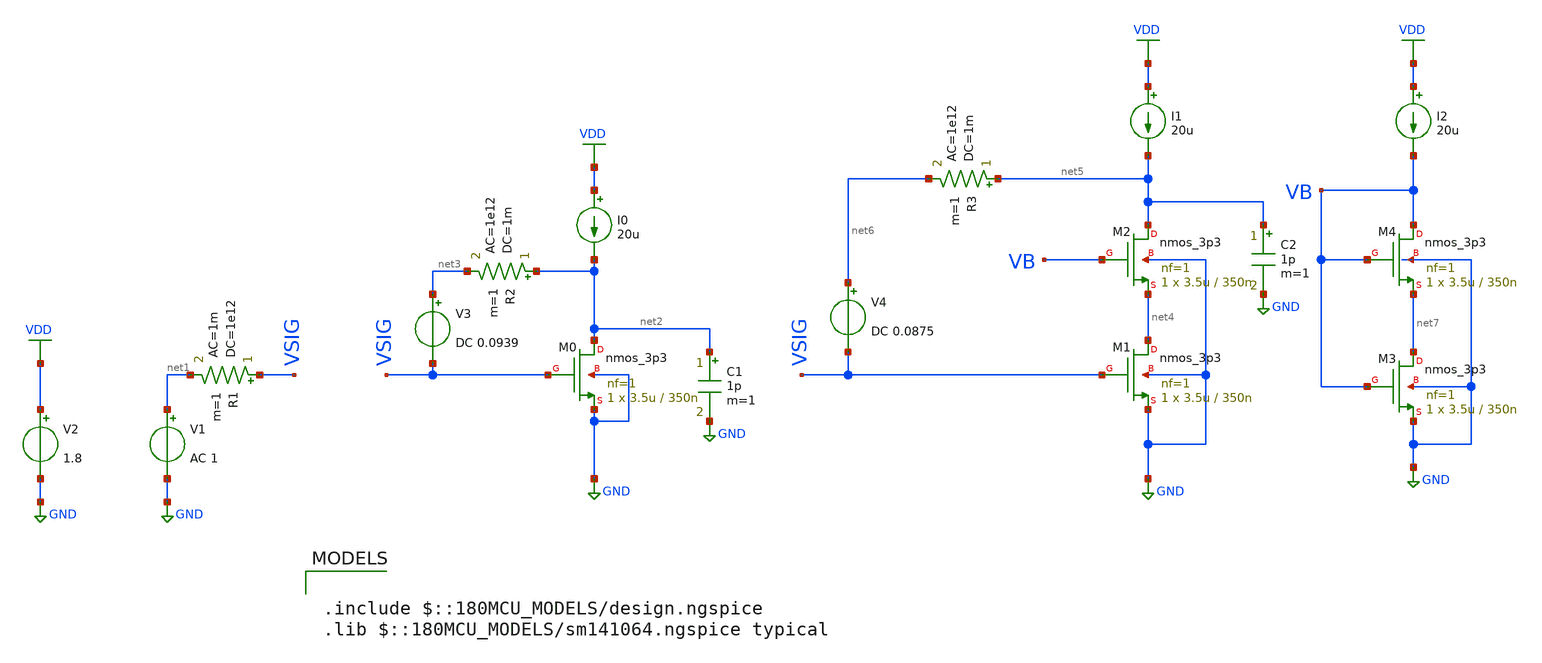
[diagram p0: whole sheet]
** sch_path: ITI_Labs/Lab3/Design/Lab03.sch
**.subckt Lab03
V1 net1 GND AC 1
R1 VSIG net1 1e12 ac=1m m=1
XM0 net2 VSIG GND GND nmos_3p3 L=350n W=3.5u nf=1 ad='int((nf+1)/2) * W/nf * 0.18u' as='int((nf+2)/2) * W/nf * 0.18u'
+ pd='2*int((nf+1)/2) * (W/nf + 0.18u)' ps='2*int((nf+2)/2) * (W/nf + 0.18u)' nrd='0.18u / W' nrs='0.18u / W'
+ sa=0 sb=0 sd=0 m=1
I0 VDD net2 20u
C1 net2 GND 1p m=1
V2 VDD GND 1.8
V3 net3 VSIG DC 0.0939
R2 net2 net3 1m ac=1e12 m=1
XM1 net4 VSIG GND GND nmos_3p3 L=350n W=3.5u nf=1 ad='int((nf+1)/2) * W/nf * 0.18u' as='int((nf+2)/2) * W/nf * 0.18u'
+ pd='2*int((nf+1)/2) * (W/nf + 0.18u)' ps='2*int((nf+2)/2) * (W/nf + 0.18u)' nrd='0.18u / W' nrs='0.18u / W'
+ sa=0 sb=0 sd=0 m=1
XM2 net5 VB net4 GND nmos_3p3 L=350n W=3.5u nf=1 ad='int((nf+1)/2) * W/nf * 0.18u' as='int((nf+2)/2) * W/nf * 0.18u'
+ pd='2*int((nf+1)/2) * (W/nf + 0.18u)' ps='2*int((nf+2)/2) * (W/nf + 0.18u)' nrd='0.18u / W' nrs='0.18u / W'
+ sa=0 sb=0 sd=0 m=1
V4 net6 VSIG DC 0.0875
I1 VDD net5 20u
R3 net5 net6 1m ac=1e12 m=1
C2 net5 GND 1p m=1
XM4 VB VB net7 GND nmos_3p3 L=350n W=3.5u nf=1 ad='int((nf+1)/2) * W/nf * 0.18u' as='int((nf+2)/2) * W/nf * 0.18u'
+ pd='2*int((nf+1)/2) * (W/nf + 0.18u)' ps='2*int((nf+2)/2) * (W/nf + 0.18u)' nrd='0.18u / W' nrs='0.18u / W'
+ sa=0 sb=0 sd=0 m=1
I2 VDD VB 20u
XM3 net7 VB GND GND nmos_3p3 L=350n W=3.5u nf=1 ad='int((nf+1)/2) * W/nf * 0.18u' as='int((nf+2)/2) * W/nf * 0.18u'
+ pd='2*int((nf+1)/2) * (W/nf + 0.18u)' ps='2*int((nf+2)/2) * (W/nf + 0.18u)' nrd='0.18u / W' nrs='0.18u / W'
+ sa=0 sb=0 sd=0 m=1
**** begin user architecture code

.include $::180MCU_MODELS/design.ngspice
.lib $::180MCU_MODELS/sm141064.ngspice typical



.control
save all  @m.xm0.m0[id]  @m.xm0.m0[vgs]  @m.xm0.m0[vds]  @m.xm0.m0[vth]  @m.xm0.m0[vdssat]
+  @m.xm0.m0[gm]  @m.xm0.m0[gds]  @m.xm0.m0[gmbs]  @m.xm0.m0[cdb]  @m.xm0.m0[cgd]  @m.xm0.m0[cgs]  @m.xm0.m0[csb]
  @m.xm1.m0[id]  @m.xm1.m0[vgs]  @m.xm1.m0[vds]  @m.xm1.m0[vth]  @m.xm1.m0[vdssat]  @m.xm1.m0[gm]
+  @m.xm1.m0[gds]  @m.xm1.m0[gmbs]  @m.xm1.m0[cdb]  @m.xm1.m0[cgd]  @m.xm1.m0[cgs]  @m.xm1.m0[csb]

  @m.xm2.m0[id]  @m.xm2.m0[vgs]  @m.xm2.m0[vds]  @m.xm2.m0[vth]  @m.xm2.m0[vdssat]  @m.xm2.m0[gm]
+  @m.xm2.m0[gds]  @m.xm2.m0[gmbs]  @m.xm2.m0[cdb]  @m.xm2.m0[cgd]  @m.xm2.m0[cgs]  @m.xm2.m0[csb]

  @m.xm3.m0[id]  @m.xm3.m0[vgs]  @m.xm3.m0[vds]  @m.xm3.m0[vth]  @m.xm3.m0[vdssat]  @m.xm3.m0[gm]
+  @m.xm3.m0[gds]  @m.xm3.m0[gmbs]  @m.xm3.m0[cdb]  @m.xm3.m0[cgd]  @m.xm3.m0[cgs]  @m.xm3.m0[csb]
  @m.xm4.m0[id]  @m.xm4.m0[vgs]  @m.xm4.m0[vds]  @m.xm4.m0[vth]  @m.xm4.m0[vdssat]  @m.xm4.m0[gm]
+  @m.xm4.m0[gds]  @m.xm4.m0[gmbs]  @m.xm4.m0[cdb]  @m.xm4.m0[cgd]  @m.xm4.m0[cgs]  @m.xm4.m0[csb]

op
print all > op_point.csv
remzerovec
set appendwrite
write Lab03.raw
.endc


**** end user architecture code
**.ends
.GLOBAL GND
.GLOBAL VDD
.end
